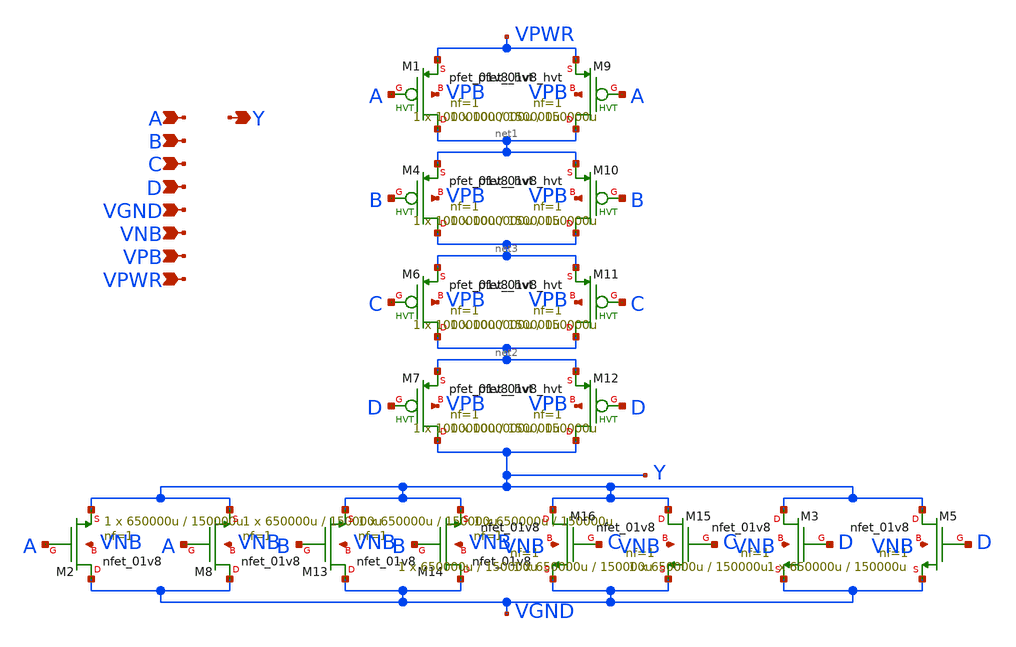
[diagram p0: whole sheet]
** sch_path: schematics/nor4/sky130_fd_sc_hd__nor4_2.sch
**.subckt sky130_fd_sc_hd__nor4_2 A B C D VGND VNB VPB VPWR Y
*.ipin A
*.ipin B
*.ipin C
*.ipin D
*.ipin VGND
*.ipin VNB
*.ipin VPB
*.ipin VPWR
*.opin Y
XM1 net1 A VPWR VPB sky130_fd_pr__pfet_01v8_hvt L=150000u W=1000000u nf=1 ad='int((1 + 1)/2) * 1000000u / 1 * 0.29'
+ as='int((1 + 2)/2) * 1000000u / 1 * 0.29' pd='2*int((1 + 1)/2) * (1000000u / 1 + 0.29)' ps='2*int((1 + 2)/2) * (1000000u / 1 + 0.29)'
+ nrd='0.29 / 1000000u ' nrs='0.29 / 1000000u ' sa=0 sb=0 sd=0 mult=1 m=1
XM2 VGND A Y VNB sky130_fd_pr__nfet_01v8 L=150000u W=650000u nf=1 ad='int((1 + 1)/2) * 650000u / 1 * 0.29'
+ as='int((1 + 2)/2) * 650000u / 1 * 0.29' pd='2*int((1 + 1)/2) * (650000u / 1 + 0.29)' ps='2*int((1 + 2)/2) * (650000u / 1 + 0.29)'
+ nrd='0.29 / 650000u ' nrs='0.29 / 650000u ' sa=0 sb=0 sd=0 mult=1 m=1
XM4 net3 B net1 VPB sky130_fd_pr__pfet_01v8_hvt L=150000u W=1000000u nf=1 ad='int((1 + 1)/2) * 1000000u / 1 * 0.29'
+ as='int((1 + 2)/2) * 1000000u / 1 * 0.29' pd='2*int((1 + 1)/2) * (1000000u / 1 + 0.29)' ps='2*int((1 + 2)/2) * (1000000u / 1 + 0.29)'
+ nrd='0.29 / 1000000u ' nrs='0.29 / 1000000u ' sa=0 sb=0 sd=0 mult=1 m=1
XM3 Y D VGND VNB sky130_fd_pr__nfet_01v8 L=150000u W=650000u nf=1 ad='int((1 + 1)/2) * 650000u / 1 * 0.29'
+ as='int((1 + 2)/2) * 650000u / 1 * 0.29' pd='2*int((1 + 1)/2) * (650000u / 1 + 0.29)' ps='2*int((1 + 2)/2) * (650000u / 1 + 0.29)'
+ nrd='0.29 / 650000u ' nrs='0.29 / 650000u ' sa=0 sb=0 sd=0 mult=1 m=1
XM5 Y D VGND VNB sky130_fd_pr__nfet_01v8 L=150000u W=650000u nf=1 ad='int((1 + 1)/2) * 650000u / 1 * 0.29'
+ as='int((1 + 2)/2) * 650000u / 1 * 0.29' pd='2*int((1 + 1)/2) * (650000u / 1 + 0.29)' ps='2*int((1 + 2)/2) * (650000u / 1 + 0.29)'
+ nrd='0.29 / 650000u ' nrs='0.29 / 650000u ' sa=0 sb=0 sd=0 mult=1 m=1
XM6 net2 C net3 VPB sky130_fd_pr__pfet_01v8_hvt L=150000u W=1000000u nf=1 ad='int((1 + 1)/2) * 1000000u / 1 * 0.29'
+ as='int((1 + 2)/2) * 1000000u / 1 * 0.29' pd='2*int((1 + 1)/2) * (1000000u / 1 + 0.29)' ps='2*int((1 + 2)/2) * (1000000u / 1 + 0.29)'
+ nrd='0.29 / 1000000u ' nrs='0.29 / 1000000u ' sa=0 sb=0 sd=0 mult=1 m=1
XM7 Y D net2 VPB sky130_fd_pr__pfet_01v8_hvt L=150000u W=1000000u nf=1 ad='int((1 + 1)/2) * 1000000u / 1 * 0.29'
+ as='int((1 + 2)/2) * 1000000u / 1 * 0.29' pd='2*int((1 + 1)/2) * (1000000u / 1 + 0.29)' ps='2*int((1 + 2)/2) * (1000000u / 1 + 0.29)'
+ nrd='0.29 / 1000000u ' nrs='0.29 / 1000000u ' sa=0 sb=0 sd=0 mult=1 m=1
XM8 VGND A Y VNB sky130_fd_pr__nfet_01v8 L=150000u W=650000u nf=1 ad='int((1 + 1)/2) * 650000u / 1 * 0.29'
+ as='int((1 + 2)/2) * 650000u / 1 * 0.29' pd='2*int((1 + 1)/2) * (650000u / 1 + 0.29)' ps='2*int((1 + 2)/2) * (650000u / 1 + 0.29)'
+ nrd='0.29 / 650000u ' nrs='0.29 / 650000u ' sa=0 sb=0 sd=0 mult=1 m=1
XM9 net1 A VPWR VPB sky130_fd_pr__pfet_01v8_hvt L=150000u W=1000000u nf=1 ad='int((1 + 1)/2) * 1000000u / 1 * 0.29'
+ as='int((1 + 2)/2) * 1000000u / 1 * 0.29' pd='2*int((1 + 1)/2) * (1000000u / 1 + 0.29)' ps='2*int((1 + 2)/2) * (1000000u / 1 + 0.29)'
+ nrd='0.29 / 1000000u ' nrs='0.29 / 1000000u ' sa=0 sb=0 sd=0 mult=1 m=1
XM10 net3 B net1 VPB sky130_fd_pr__pfet_01v8_hvt L=150000u W=1000000u nf=1 ad='int((1 + 1)/2) * 1000000u / 1 * 0.29'
+ as='int((1 + 2)/2) * 1000000u / 1 * 0.29' pd='2*int((1 + 1)/2) * (1000000u / 1 + 0.29)' ps='2*int((1 + 2)/2) * (1000000u / 1 + 0.29)'
+ nrd='0.29 / 1000000u ' nrs='0.29 / 1000000u ' sa=0 sb=0 sd=0 mult=1 m=1
XM11 net2 C net3 VPB sky130_fd_pr__pfet_01v8_hvt L=150000u W=1000000u nf=1 ad='int((1 + 1)/2) * 1000000u / 1 * 0.29'
+ as='int((1 + 2)/2) * 1000000u / 1 * 0.29' pd='2*int((1 + 1)/2) * (1000000u / 1 + 0.29)' ps='2*int((1 + 2)/2) * (1000000u / 1 + 0.29)'
+ nrd='0.29 / 1000000u ' nrs='0.29 / 1000000u ' sa=0 sb=0 sd=0 mult=1 m=1
XM12 Y D net2 VPB sky130_fd_pr__pfet_01v8_hvt L=150000u W=1000000u nf=1 ad='int((1 + 1)/2) * 1000000u / 1 * 0.29'
+ as='int((1 + 2)/2) * 1000000u / 1 * 0.29' pd='2*int((1 + 1)/2) * (1000000u / 1 + 0.29)' ps='2*int((1 + 2)/2) * (1000000u / 1 + 0.29)'
+ nrd='0.29 / 1000000u ' nrs='0.29 / 1000000u ' sa=0 sb=0 sd=0 mult=1 m=1
XM13 VGND B Y VNB sky130_fd_pr__nfet_01v8 L=150000u W=650000u nf=1 ad='int((1 + 1)/2) * 650000u / 1 * 0.29'
+ as='int((1 + 2)/2) * 650000u / 1 * 0.29' pd='2*int((1 + 1)/2) * (650000u / 1 + 0.29)' ps='2*int((1 + 2)/2) * (650000u / 1 + 0.29)'
+ nrd='0.29 / 650000u ' nrs='0.29 / 650000u ' sa=0 sb=0 sd=0 mult=1 m=1
XM14 VGND B Y VNB sky130_fd_pr__nfet_01v8 L=150000u W=650000u nf=1 ad='int((1 + 1)/2) * 650000u / 1 * 0.29'
+ as='int((1 + 2)/2) * 650000u / 1 * 0.29' pd='2*int((1 + 1)/2) * (650000u / 1 + 0.29)' ps='2*int((1 + 2)/2) * (650000u / 1 + 0.29)'
+ nrd='0.29 / 650000u ' nrs='0.29 / 650000u ' sa=0 sb=0 sd=0 mult=1 m=1
XM15 Y C VGND VNB sky130_fd_pr__nfet_01v8 L=150000u W=650000u nf=1 ad='int((1 + 1)/2) * 650000u / 1 * 0.29'
+ as='int((1 + 2)/2) * 650000u / 1 * 0.29' pd='2*int((1 + 1)/2) * (650000u / 1 + 0.29)' ps='2*int((1 + 2)/2) * (650000u / 1 + 0.29)'
+ nrd='0.29 / 650000u ' nrs='0.29 / 650000u ' sa=0 sb=0 sd=0 mult=1 m=1
XM16 Y C VGND VNB sky130_fd_pr__nfet_01v8 L=150000u W=650000u nf=1 ad='int((1 + 1)/2) * 650000u / 1 * 0.29'
+ as='int((1 + 2)/2) * 650000u / 1 * 0.29' pd='2*int((1 + 1)/2) * (650000u / 1 + 0.29)' ps='2*int((1 + 2)/2) * (650000u / 1 + 0.29)'
+ nrd='0.29 / 650000u ' nrs='0.29 / 650000u ' sa=0 sb=0 sd=0 mult=1 m=1
**.ends
.end
